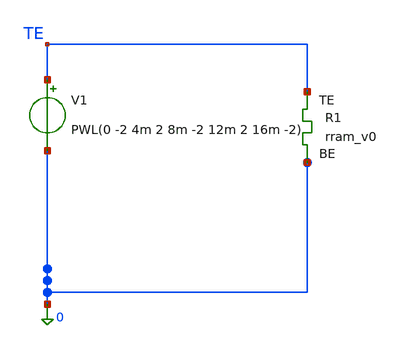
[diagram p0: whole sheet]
** sch_path: memristor_models/wellposed/tb_liss_rram_v0.sch
**.subckt tb_liss_rram_v0
V1 TE 0 PWL(0 -2 4m 2 8m -2 12m 2 16m -2)
XR1 TE 0 rram_v0
**** begin user architecture code

** opencircuitdesign pdks install
.inc $::SKYWATER_MODELS/rram_v0.spice



.option savecurrents
.tran 100n 16m
.control
	save all
	run
	write tb_liss_rram_v0.raw
.endc



**** end user architecture code
**.ends
.end
